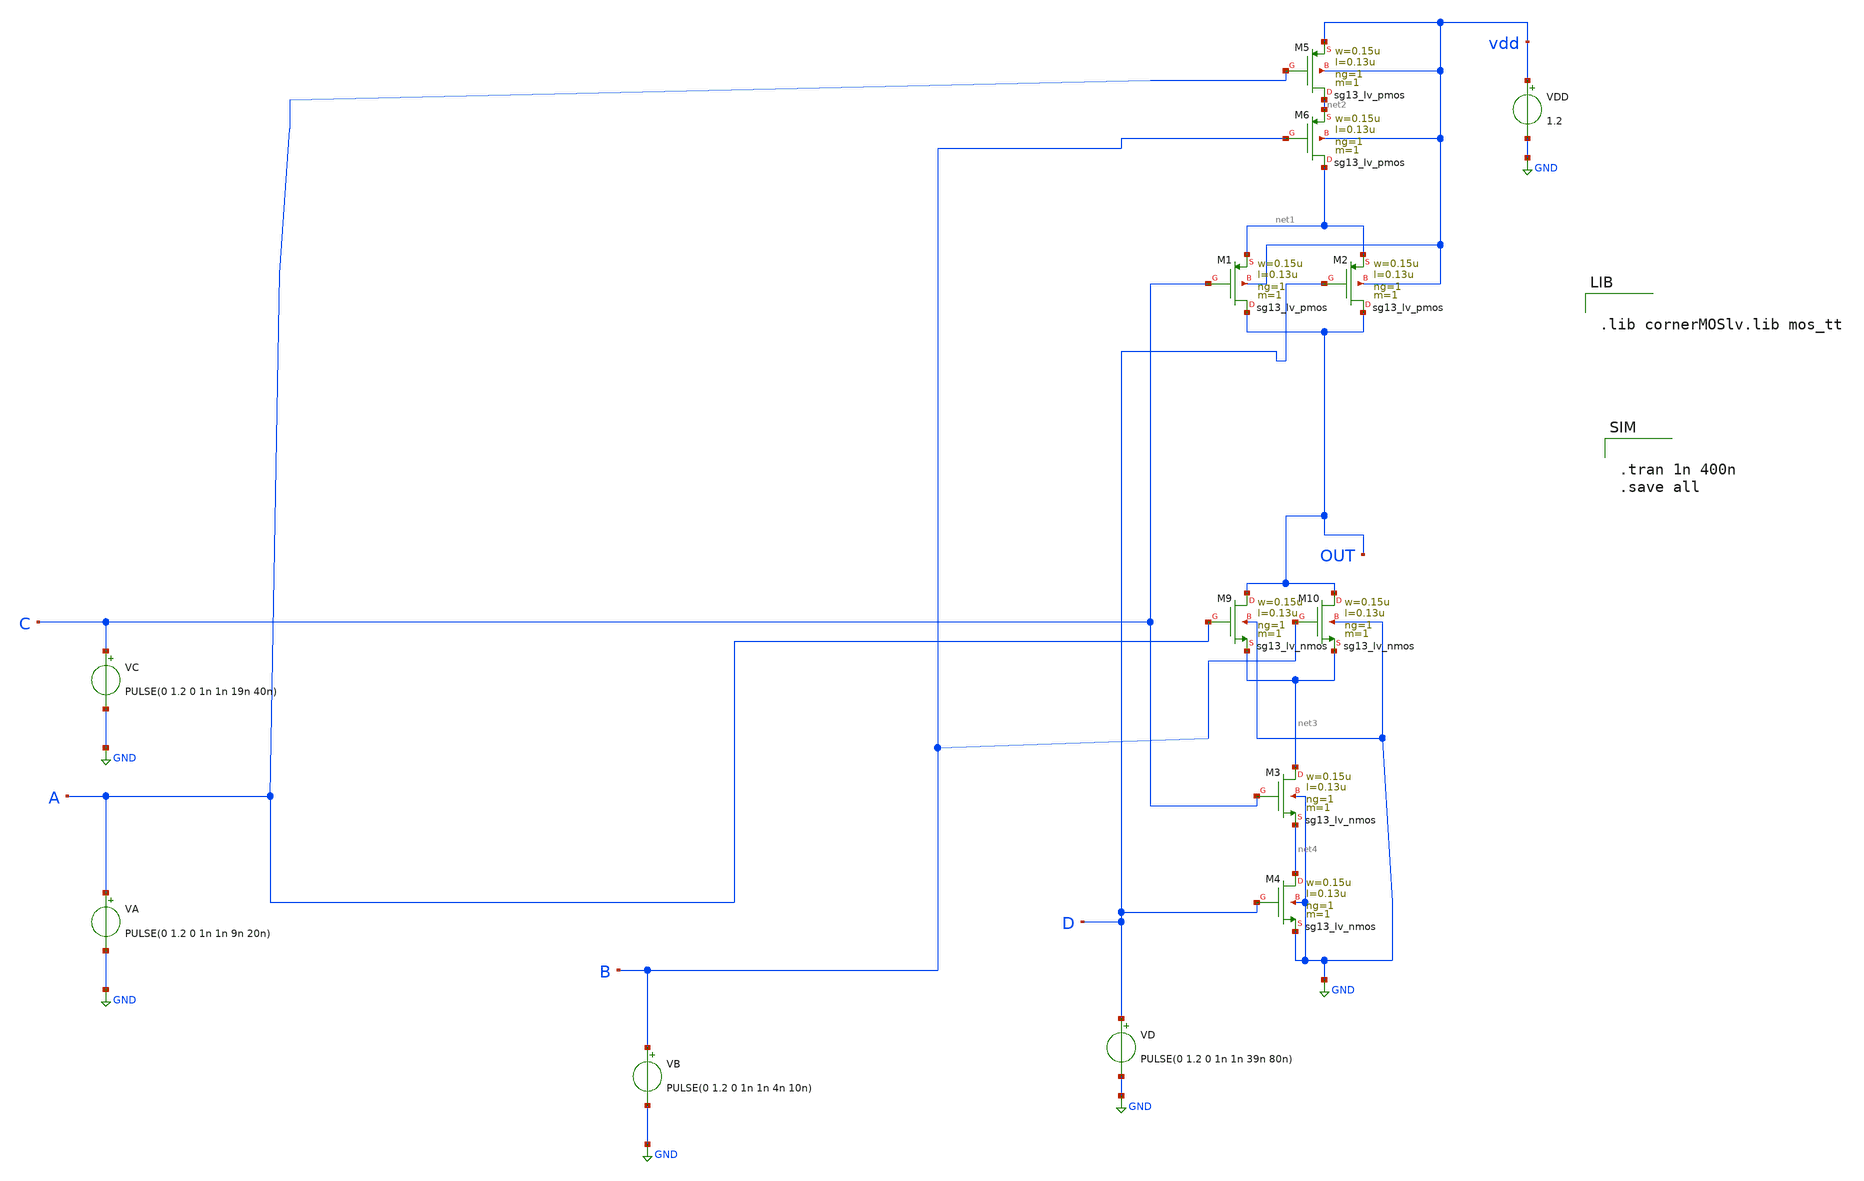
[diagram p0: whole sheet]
** sch_path: oai211.sch
**.subckt oai211
XM1 OUT C net1 vdd sg13_lv_pmos w=0.15u l=0.13u ng=1 m=1 mm_ok=1
XM2 OUT D net1 vdd sg13_lv_pmos w=0.15u l=0.13u ng=1 m=1 mm_ok=1
VDD vdd GND 1.2
VA A GND PULSE(0 1.2 0 1n 1n 9n 20n)
VB B GND PULSE(0 1.2 0 1n 1n 4n 10n)
VC C GND PULSE(0 1.2 0 1n 1n 19n 40n)
VD D GND PULSE(0 1.2 0 1n 1n 39n 80n)
XM5 net2 A vdd vdd sg13_lv_pmos w=0.15u l=0.13u ng=1 m=1 mm_ok=1
XM6 net1 B net2 vdd sg13_lv_pmos w=0.15u l=0.13u ng=1 m=1 mm_ok=1
XM9 OUT A net3 GND sg13_lv_nmos w=0.15u l=0.13u ng=1 m=1 mm_ok=1
XM10 OUT B net3 GND sg13_lv_nmos w=0.15u l=0.13u ng=1 m=1 mm_ok=1
XM3 net3 C net4 GND sg13_lv_nmos w=0.15u l=0.13u ng=1 m=1 mm_ok=1
XM4 net4 D GND GND sg13_lv_nmos w=0.15u l=0.13u ng=1 m=1 mm_ok=1
**** begin user architecture code


.lib cornerMOSlv.lib mos_tt



.tran 1n 400n
.save all


**** end user architecture code
**.ends
.GLOBAL GND
.end
